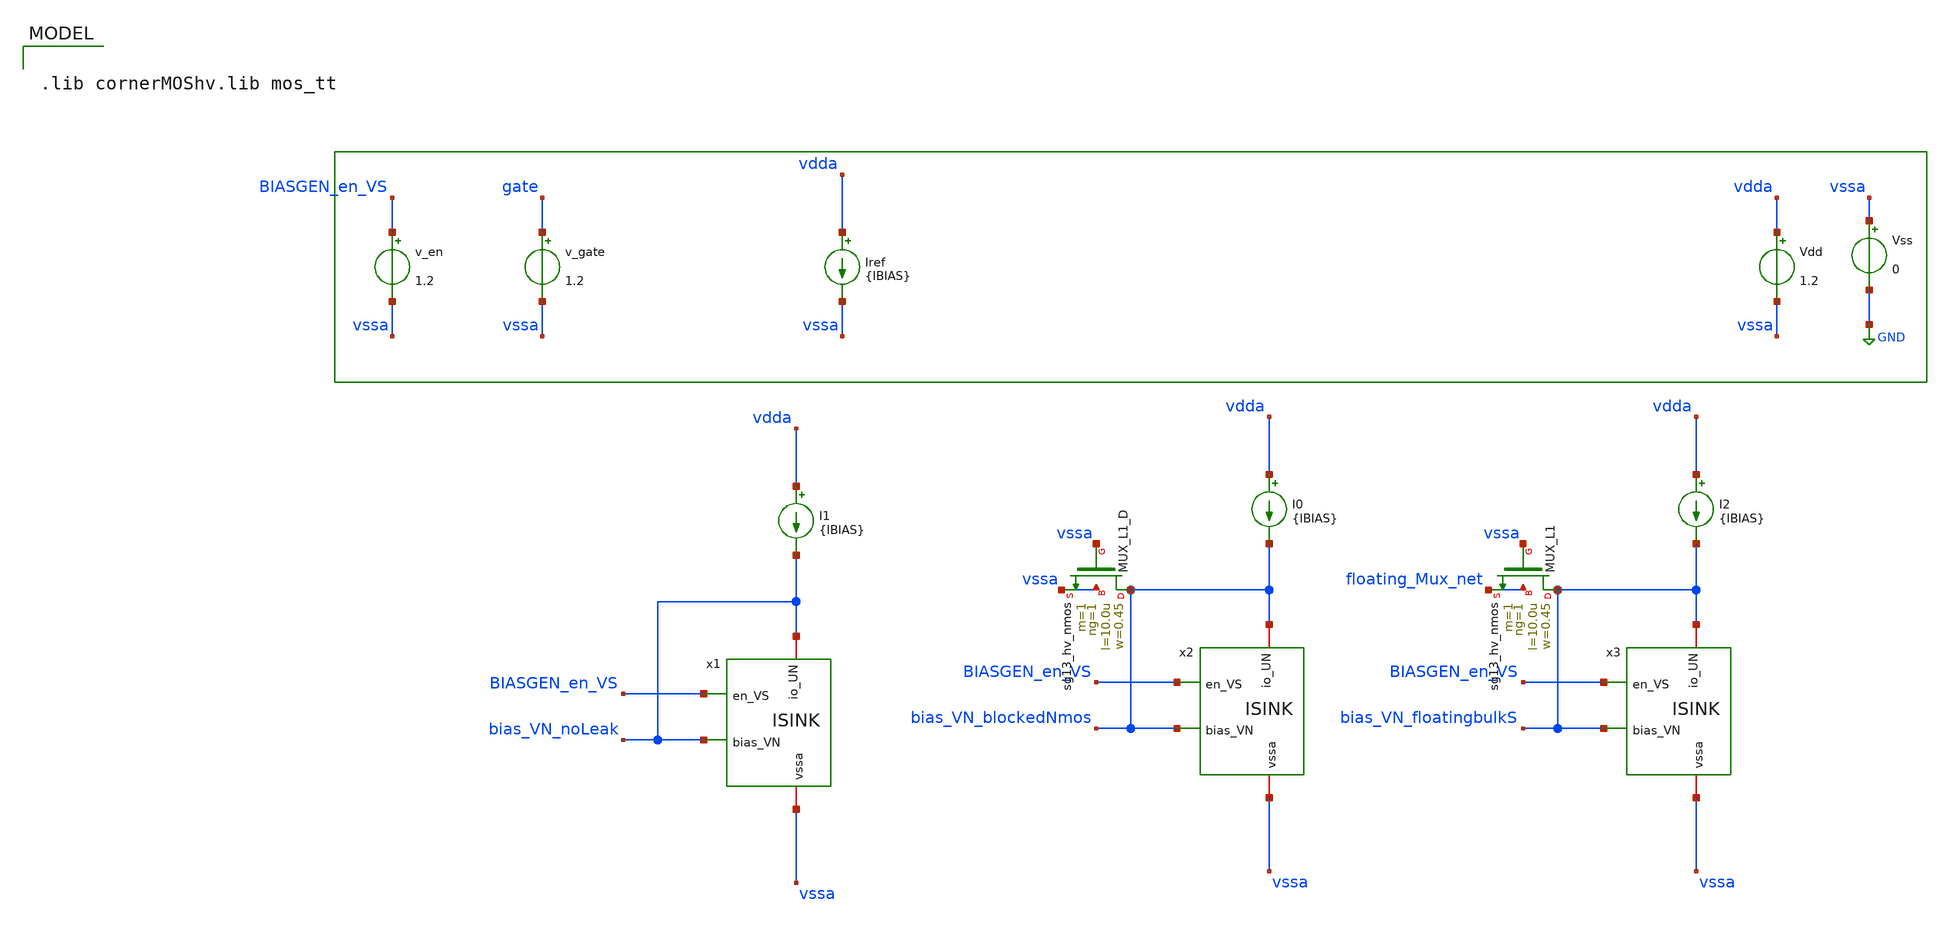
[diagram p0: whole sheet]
** sch_path: test_bench/ISINK_dc_tb.sch
**.subckt ISINK_dc_tb
v_en BIASGEN_en_VS vssa 1.2
Vdd vdda vssa 1.2
Vss vssa GND 0
x2 bias_VN_blockedNmos vssa BIASGEN_en_VS bias_VN_blockedNmos ISINK
I0 vdda bias_VN_blockedNmos {IBIAS}
XMUX_L1_D bias_VN_blockedNmos vssa vssa vssa sg13_hv_nmos w=0.45 l=10.0u ng=1 m=1 mm_ok=1
v_gate gate vssa 1.2
x1 bias_VN_noLeak vssa BIASGEN_en_VS bias_VN_noLeak ISINK
I1 vdda bias_VN_noLeak {IBIAS}
x3 bias_VN_floatingbulkS vssa BIASGEN_en_VS bias_VN_floatingbulkS ISINK
I2 vdda bias_VN_floatingbulkS {IBIAS}
XMUX_L1 bias_VN_floatingbulkS vssa floating_Mux_net floating_Mux_net sg13_hv_nmos w=0.45 l=10.0u
+ ng=1 m=1 mm_ok=1
Iref vdda vssa {IBIAS}
**** begin user architecture code

.lib cornerMOShv.lib mos_tt



.param temp=27
.param IBIAS=1m

.options abstol=1e-14
.options gmin=1e-14
.control
save all
    dc I2 10p 1u 10p

    write ISINK_floatingbulkS_dc_tb.raw
    plot V(bias_VN_floatingbulkS)

.endc


**** end user architecture code
**.ends

* expanding   symbol:  ISINK.sym # of pins=4
** sym_path: test_bench/ISINK.sym
** sch_path: test_bench/ISINK.sch
.subckt ISINK bias_VN vssa en_VS io_UN
*.ipin en_VS
*.iopin vssa
*.ipin bias_VN
*.iopin io_UN
XM1 io_UN en_VS net2 vssa sg13_hv_nmos w=2.5u l=0.5u ng=1 m=1 mm_ok=1
XM2 net2 bias_VN net1 vssa sg13_hv_nmos w=1u l=2u ng=1 m=1 mm_ok=1
XM3 net1 bias_VN vssa vssa sg13_hv_nmos w=1u l=2u ng=1 m=1 mm_ok=1
.ends

.GLOBAL GND
.end
